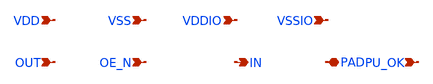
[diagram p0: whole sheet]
** sch_path: sch/pads/sky130/sdr_bidir_pad.sch
**.subckt sdr_bidir_pad OUT OE_N IN PAD PU_OK VDD VSS VDDIO VSSIO
*.ipin OUT
*.ipin OE_N
*.opin IN
*.iopin PAD
*.ipin PU_OK
*.ipin VDD
*.ipin VSS
*.ipin VDDIO
*.ipin VSSIO
**** begin user architecture code


* GENERATED by generator/emit_pads.py -- DO NOT EDIT BY HAND
* backend: sky130   pdk: sky130A
* topology: specs/pads/topology.yaml v1 -- ONE shared schematic, only device names change
* STATUS: topology_template_only
* license: Apache-2.0 (SkyWater PDK Authors)
* SIZE UNITS: topology params are metres; sky130 subckts use .option scale=1u (micrometres), apply
*+ x1e6 when filling
* ESD NOTE: 2-terminal .model diodes; area unit and clamp orientation still need schematic review
*
* NOT SIMULATABLE. This is a TOPOLOGY TEMPLATE:
*   - every W / L / NF / R / area is an unresolved parameter
*     (see required_params.json). ngspice rejects them until filled.
*   - PAD_OE_CTRL is a generated transistor-level block (IO gates plus
*     an optional core-to-IO level shifter); its devices reuse the
*     pre-driver sizing placeholders and are not optimized.
*   - diode orientation, bulk ties and the series-R third terminal must
*     be confirmed at schematic review; they are NOT signed off here.
*   - L_R_SERIES is the on-chip resistor LENGTH. The target
*     resistance in ohm is a board-level SI input, not a pad param;
*     converting target R to L needs a per-PDK sheet resistance.
*
* Device-instantiation syntax is per backend (nf vs ng, m vs mr,
* r_length/r_width vs w/l, 2-terminal diode model vs 3-terminal ESD
* subckt). It lives in specs/pads/devices/<backend>.yaml; the block
* topology below stays shared.
*
* Expected includes (NOT bundled; integrator supplies models.spice):
*   libs.tech/ngspice/sky130.lib.spice (corner section tt/ss/ff)
*   none (device models only)
*
* Shared signal chain (docs/ARCHITECTURE.md section 5):
*   OUT/OE_N --[level shift if VDD != VDDIO]--> pre-driver --> tri-state
*   --> series R --> PAD --> ESD (to VDDIO / VSSIO + power clamp)
*   PAD --> CMOS/Schmitt RX --> [level shift back] --> IN
*   power-up Hi-Z until VDD and VDDIO are both present (PU_OK)

X_INV_P Y A VDDIO VDDIO sky130_fd_pr__pfet_g5v0d10v5 w=W_P_PDRV l=L_PDRV nf=NF_DEVICE m=M_DEVICE
X_INV_N Y A VSSIO VSSIO sky130_fd_pr__nfet_g5v0d10v5 w=W_N_PDRV l=L_PDRV nf=NF_DEVICE m=M_DEVICE
X_NAND_P1 Y A VDDIO VDDIO sky130_fd_pr__pfet_g5v0d10v5 w=W_P_PDRV l=L_PDRV nf=NF_DEVICE m=M_DEVICE
X_NAND_P2 Y B VDDIO VDDIO sky130_fd_pr__pfet_g5v0d10v5 w=W_P_PDRV l=L_PDRV nf=NF_DEVICE m=M_DEVICE
X_NAND_N1 Y A nand_mid VSSIO sky130_fd_pr__nfet_g5v0d10v5 w=W_N_PDRV l=L_PDRV nf=NF_DEVICE
+ m=M_DEVICE
X_NAND_N2 nand_mid B VSSIO VSSIO sky130_fd_pr__nfet_g5v0d10v5 w=W_N_PDRV l=L_PDRV nf=NF_DEVICE
+ m=M_DEVICE
X_NOR_P1 Y A nor_mid VDDIO sky130_fd_pr__pfet_g5v0d10v5 w=W_P_PDRV l=L_PDRV nf=NF_DEVICE m=M_DEVICE
X_NOR_P2 nor_mid B VDDIO VDDIO sky130_fd_pr__pfet_g5v0d10v5 w=W_P_PDRV l=L_PDRV nf=NF_DEVICE
+ m=M_DEVICE
X_NOR_N1 Y A VSSIO VSSIO sky130_fd_pr__nfet_g5v0d10v5 w=W_N_PDRV l=L_PDRV nf=NF_DEVICE m=M_DEVICE
X_NOR_N2 Y B VSSIO VSSIO sky130_fd_pr__nfet_g5v0d10v5 w=W_N_PDRV l=L_PDRV nf=NF_DEVICE m=M_DEVICE
X_LS_INV_P INB IN VDD VDD sky130_fd_pr__pfet_01v8 w=W_P_PDRV l=L_PDRV nf=NF_DEVICE m=M_DEVICE
X_LS_INV_N INB IN VSS VSS sky130_fd_pr__nfet_01v8 w=W_N_PDRV l=L_PDRV nf=NF_DEVICE m=M_DEVICE
X_LS_N1 OUTB IN VSSIO VSSIO sky130_fd_pr__nfet_g5v0d10v5 w=W_N_PDRV*16 l=L_PDRV nf=NF_DEVICE
+ m=M_DEVICE
X_LS_N2 OUT INB VSSIO VSSIO sky130_fd_pr__nfet_g5v0d10v5 w=W_N_PDRV*16 l=L_PDRV nf=NF_DEVICE
+ m=M_DEVICE
X_LS_P1 OUTB OUT VDDIO VDDIO sky130_fd_pr__pfet_g5v0d10v5 w=W_P_PDRV l=L_PDRV nf=NF_DEVICE
+ m=M_DEVICE
X_LS_P2 OUT OUTB VDDIO VDDIO sky130_fd_pr__pfet_g5v0d10v5 w=W_P_PDRV l=L_PDRV nf=NF_DEVICE
+ m=M_DEVICE
X_LS OUT OUT_I OUTB_I VDD VSS VDDIO VSSIO LS_C2I
* OE_N and PU_OK are IO-domain control inputs in this macro
X_INV_OE OE_N OENB VDDIO VSSIO INV_IO
X_NAND PU_OK OENB EN_N VDDIO VSSIO NAND2_IO
X_NOR_GN EN_N OUT_I N_GN VDDIO VSSIO NOR2_IO
X_NOR_GP EN_N OUTB_I NGPB VDDIO VSSIO NOR2_IO
X_INV_NGP NGPB N_GP VDDIO VSSIO INV_IO


* --- OE / power-up gating: real transistor-level block (see header) ---
X_OE_CTRL n_gp n_gn OUT OE_N PU_OK VDD VSS VDDIO VSSIO PAD_OE_CTRL

* --- pre-driver chain (even stage count preserves polarity) ---
X_PDRV_P_GP1 n_gp_s1 n_gp VDDIO VDDIO sky130_fd_pr__pfet_g5v0d10v5 w=W_P_PDRV l=L_PDRV nf=NF_DEVICE
+ m=M_DEVICE
X_PDRV_N_GP1 n_gp_s1 n_gp VSSIO VSSIO sky130_fd_pr__nfet_g5v0d10v5 w=W_N_PDRV l=L_PDRV nf=NF_DEVICE
+ m=M_DEVICE
X_PDRV_P_GP2 n_gp_drv n_gp_s1 VDDIO VDDIO sky130_fd_pr__pfet_g5v0d10v5 w=W_P_PDRV l=L_PDRV
+ nf=NF_DEVICE m=M_DEVICE
X_PDRV_N_GP2 n_gp_drv n_gp_s1 VSSIO VSSIO sky130_fd_pr__nfet_g5v0d10v5 w=W_N_PDRV l=L_PDRV
+ nf=NF_DEVICE m=M_DEVICE
X_PDRV_P_GN1 n_gn_s1 n_gn VDDIO VDDIO sky130_fd_pr__pfet_g5v0d10v5 w=W_P_PDRV l=L_PDRV nf=NF_DEVICE
+ m=M_DEVICE
X_PDRV_N_GN1 n_gn_s1 n_gn VSSIO VSSIO sky130_fd_pr__nfet_g5v0d10v5 w=W_N_PDRV l=L_PDRV nf=NF_DEVICE
+ m=M_DEVICE
X_PDRV_P_GN2 n_gn_drv n_gn_s1 VDDIO VDDIO sky130_fd_pr__pfet_g5v0d10v5 w=W_P_PDRV l=L_PDRV
+ nf=NF_DEVICE m=M_DEVICE
X_PDRV_N_GN2 n_gn_drv n_gn_s1 VSSIO VSSIO sky130_fd_pr__nfet_g5v0d10v5 w=W_N_PDRV l=L_PDRV
+ nf=NF_DEVICE m=M_DEVICE

* --- tri-state output (PMOS to VDDIO, NMOS to VSSIO) ---
X_OUT_P n_pre n_gp_drv VDDIO VDDIO sky130_fd_pr__pfet_g5v0d10v5 w=W_P_OUT l=L_P_OUT nf=NF_P_OUT
+ m=M_DEVICE
X_OUT_N n_pre n_gn_drv VSSIO VSSIO sky130_fd_pr__nfet_g5v0d10v5 w=W_N_OUT l=L_N_OUT nf=NF_N_OUT
+ m=M_DEVICE

* --- on-chip series damping resistor (may instead live on the board) ---
X_RSER n_pre PAD VSSIO sky130_fd_pr__res_high_po w=W_R_SERIES l=L_R_SERIES

* --- ESD: primary diodes + VDDIO-to-VSSIO clamp ---
D_ESD_UP PAD VDDIO sky130_fd_pr__diode_pd2nw_11v0 area=ESD_AREA_UP
D_ESD_DN VSSIO PAD sky130_fd_pr__diode_pw2nd_11v0 area=ESD_AREA_DN
D_CLAMP VSSIO VDDIO sky130_fd_pr__diode_pd2nw_11v0 area=ESD_CLAMP_W

* --- SDR receiver: thick-oxide CMOS inverter (Schmitt optional) ---
X_RX_N IN PAD VSSIO VSSIO sky130_fd_pr__nfet_g5v0d10v5 w=W_RX_N l=L_PDRV nf=NF_DEVICE m=M_DEVICE
X_RX_P IN PAD VDDIO VDDIO sky130_fd_pr__pfet_g5v0d10v5 w=W_RX_P l=L_PDRV nf=NF_DEVICE m=M_DEVICE
* RX_HYST unresolved; do NOT assume the input threshold equals VDDIO/2.

* --- IO -> core level shifter for IN: topology TBD (not a drawn netlist) ---

* --- guard ring surrounds output stage and ESD (layout only) ---
* GUARD_RING_WIDTH / GUARD_RING_SPACING unresolved; not drawn here.


**** end user architecture code
**.ends
.end
